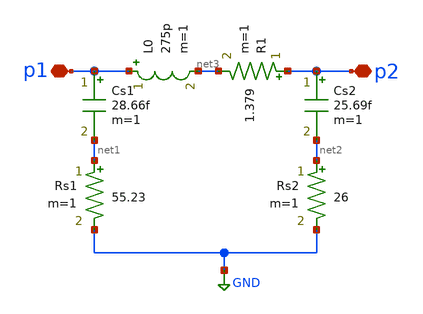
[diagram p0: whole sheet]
** sch_path: impedance-transformer/xschem/l1.sch
**.subckt l1 p2 p1
*.iopin p2
*.iopin p1
L0 p1 net3 275p m=1
Cs1 p1 net1 28.66f m=1
Cs2 p2 net2 25.69f m=1
Rs1 net1 GND 55.23 m=1
Rs2 net2 GND 26 m=1
R1 p2 net3 1.379 m=1
**.ends
.GLOBAL GND
.end
